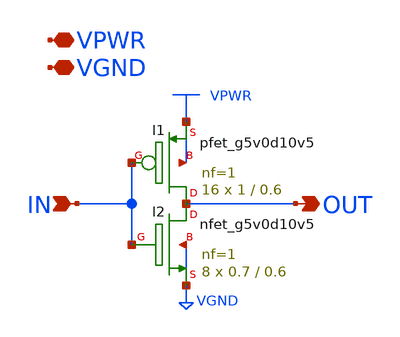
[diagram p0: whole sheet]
** sch_path: common/hvsbt_inv_x8.sch
* Copyright 2023 David Mitchell Bailey
* Licensed under the Apache License, Version 2.0 (the "License");
* you may not use this file except in compliance with the License.
* You may obtain a copy of the License at
* https://www.apache.org/licenses/LICENSE-2.0
* Unless required by applicable law or agreed to in writing, software
* distributed under the License is distributed on an "AS IS" BASIS,
* WITHOUT WARRANTIES OR CONDITIONS OF ANY KIND, either express or implied.
* See the License for the specific language governing permissions and
* limitations under the License.
**.subckt hvsbt_inv_x8 IN OUT VPWR VGND
*.ipin IN
*.opin OUT
*.iopin VPWR
*.iopin VGND
XI2 OUT IN VGND VGND sky130_fd_pr__nfet_g5v0d10v5 L=0.6 W=0.7 nf=1 ad='int((nf+1)/2) * W/nf * 0.29' as='int((nf+2)/2) * W/nf * 0.29'
+ pd='2*int((nf+1)/2) * (W/nf + 0.29)' ps='2*int((nf+2)/2) * (W/nf + 0.29)' nrd='0.29 / W' nrs='0.29 / W'
+ sa=0 sb=0 sd=0 mult=8 m=8
XI1 OUT IN VPWR VPWR sky130_fd_pr__pfet_g5v0d10v5 L=0.6 W=1 nf=1 ad='int((nf+1)/2) * W/nf * 0.29' as='int((nf+2)/2) * W/nf * 0.29'
+ pd='2*int((nf+1)/2) * (W/nf + 0.29)' ps='2*int((nf+2)/2) * (W/nf + 0.29)' nrd='0.29 / W' nrs='0.29 / W'
+ sa=0 sb=0 sd=0 mult=16 m=16
**.ends
.end
